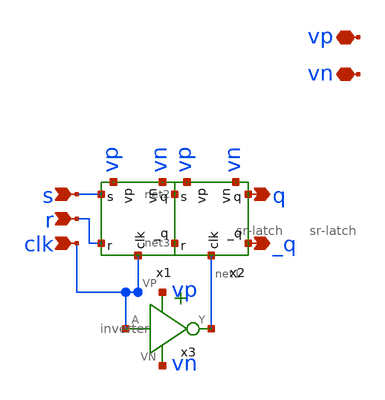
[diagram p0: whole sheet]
** sch_path: xschem/logic_gates/sr-flipflop.sch
**.subckt sr-flipflop vp vn s r clk q _q
*.iopin vp
*.iopin vn
*.ipin s
*.ipin r
*.ipin clk
*.opin q
*.opin _q
x1 vp vn s net2 r net3 clk sr-latch
x2 vp vn net2 q net3 _q net1 sr-latch
x3 vp clk net1 vn inverter
**.ends
.end
